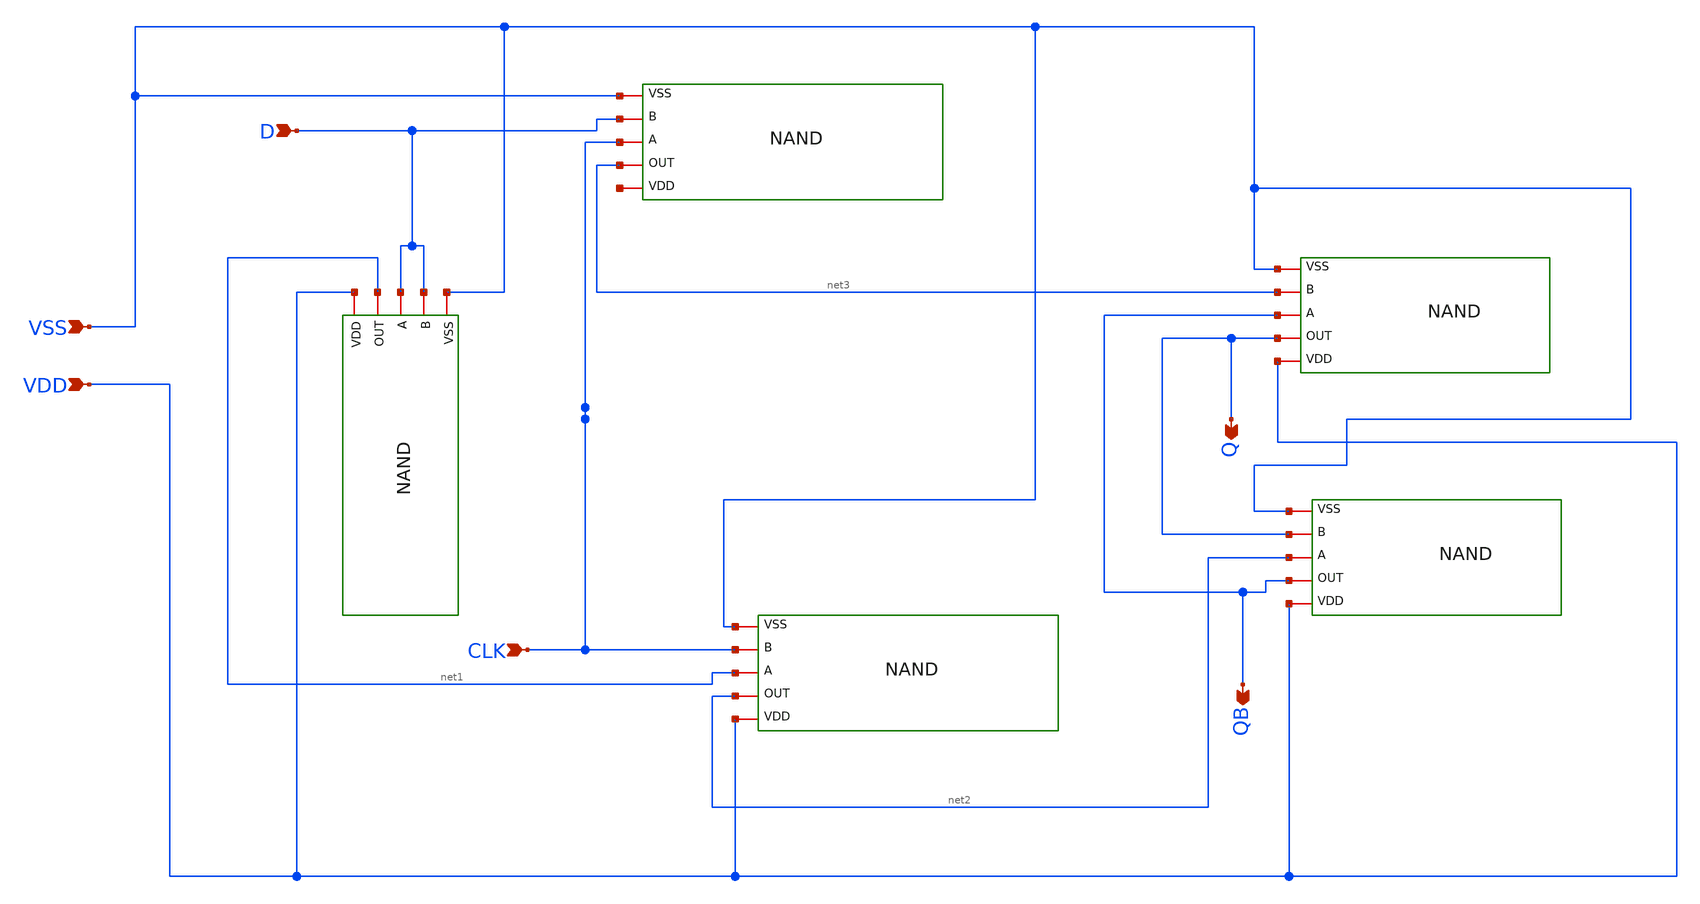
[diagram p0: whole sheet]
** sch_path: designs/libs/core_analog/DFF/DFF.sch
**.subckt DFF D VSS VDD Q QB CLK
*.ipin D
*.ipin VSS
*.ipin VDD
*.opin Q
*.opin QB
*.ipin CLK
x1 VDD net1 D D VSS NAND
x2 net4 net3 CLK D VSS NAND
x3 VDD net2 net1 CLK VSS NAND
x4 VDD Q QB net3 VSS NAND
x5 VDD QB net2 Q VSS NAND
**.ends
.end
